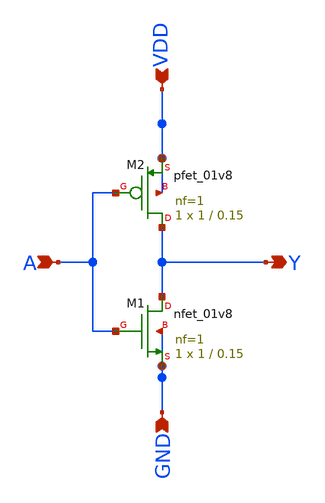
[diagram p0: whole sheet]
** sch_path: Work/work-1/untitled-1.sch
**.subckt untitled-1 A VDD GND Y
*.ipin A
*.ipin VDD
*.ipin GND
*.opin Y
XM1 Y A GND GND sky130_fd_pr__nfet_01v8 L=0.15 W=1 nf=1 ad='int((1 + 1)/2) * 1 / 1 * 0.29' as='int((1 + 2)/2) * 1 / 1 * 0.29'
+ pd='2*int((1 + 1)/2) * (1 / 1 + 0.29)' ps='2*int((1 + 2)/2) * (1 / 1 + 0.29)' nrd='0.29 / 1 ' nrs='0.29 / 1 '
+ sa=0 sb=0 sd=0 mult=1 m=1
XM2 Y A VDD VDD sky130_fd_pr__pfet_01v8 L=0.15 W=1 nf=1 ad='int((1 + 1)/2) * 1 / 1 * 0.29' as='int((1 + 2)/2) * 1 / 1 * 0.29'
+ pd='2*int((1 + 1)/2) * (1 / 1 + 0.29)' ps='2*int((1 + 2)/2) * (1 / 1 + 0.29)' nrd='0.29 / 1 ' nrs='0.29 / 1 '
+ sa=0 sb=0 sd=0 mult=1 m=1
**** begin user architecture code
.lib /usr/local/share/pdk/sky130A/libs.tech/ngspice/sky130.lib.spice tt
**** end user architecture code
**.ends
.end
